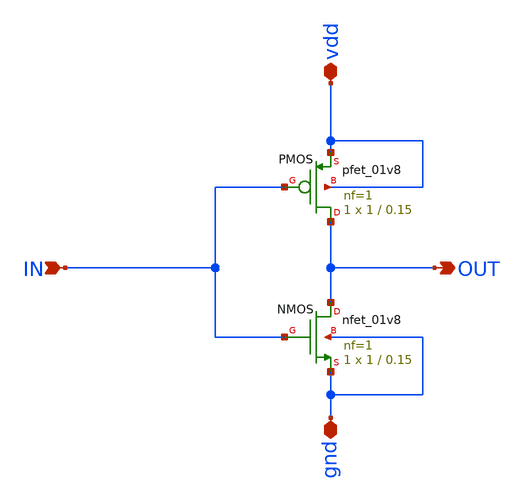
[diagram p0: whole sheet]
** sch_path: Week_0/Inverter_PreLayout/Inverter_sym.sch
**.subckt Inverter_sym OUT IN vdd gnd
*.opin OUT
*.ipin IN
*.iopin vdd
*.iopin gnd
XPMOS OUT IN vdd vdd sky130_fd_pr__pfet_01v8 L=0.15 W=1 nf=1 ad='int((nf+1)/2) * W/nf * 0.29' as='int((nf+2)/2) * W/nf * 0.29'
+ pd='2*int((nf+1)/2) * (W/nf + 0.29)' ps='2*int((nf+2)/2) * (W/nf + 0.29)' nrd='0.29 / W' nrs='0.29 / W'
+ sa=0 sb=0 sd=0 mult=1 m=1
XNMOS OUT IN gnd gnd sky130_fd_pr__nfet_01v8 L=0.15 W=1 nf=1 ad='int((nf+1)/2) * W/nf * 0.29' as='int((nf+2)/2) * W/nf * 0.29'
+ pd='2*int((nf+1)/2) * (W/nf + 0.29)' ps='2*int((nf+2)/2) * (W/nf + 0.29)' nrd='0.29 / W' nrs='0.29 / W'
+ sa=0 sb=0 sd=0 mult=1 m=1
**.ends
.end
